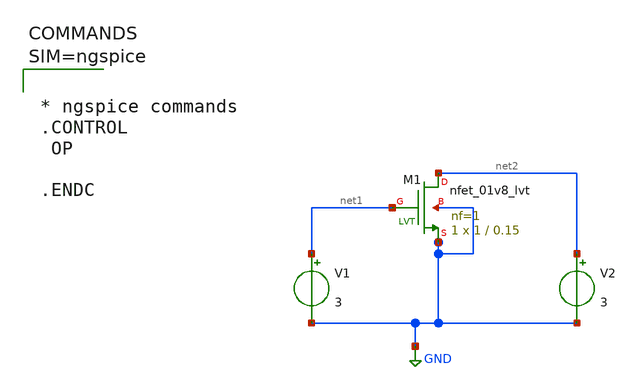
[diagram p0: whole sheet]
** sch_path: work/xschem/untitled-1.sch
**.subckt untitled-1
XM1 net2 net1 GND GND sky130_fd_pr__nfet_01v8_lvt L=0.15 W=1 nf=1 ad='int((1 + 1)/2) * 1 / 1 * 0.29'
+ as='int((1 + 2)/2) * 1 / 1 * 0.29' pd='2*int((1 + 1)/2) * (1 / 1 + 0.29)' ps='2*int((1 + 2)/2) * (1 / 1 + 0.29)'
+ nrd='0.29 / 1 ' nrs='0.29 / 1 ' sa=0 sb=0 sd=0 mult=1 m=1
V1 net1 GND 3
V2 net2 GND 3
**** begin user architecture code



* ngspice commands
.CONTROL
 OP

.ENDC



**** end user architecture code
**.ends
.GLOBAL GND
.end
